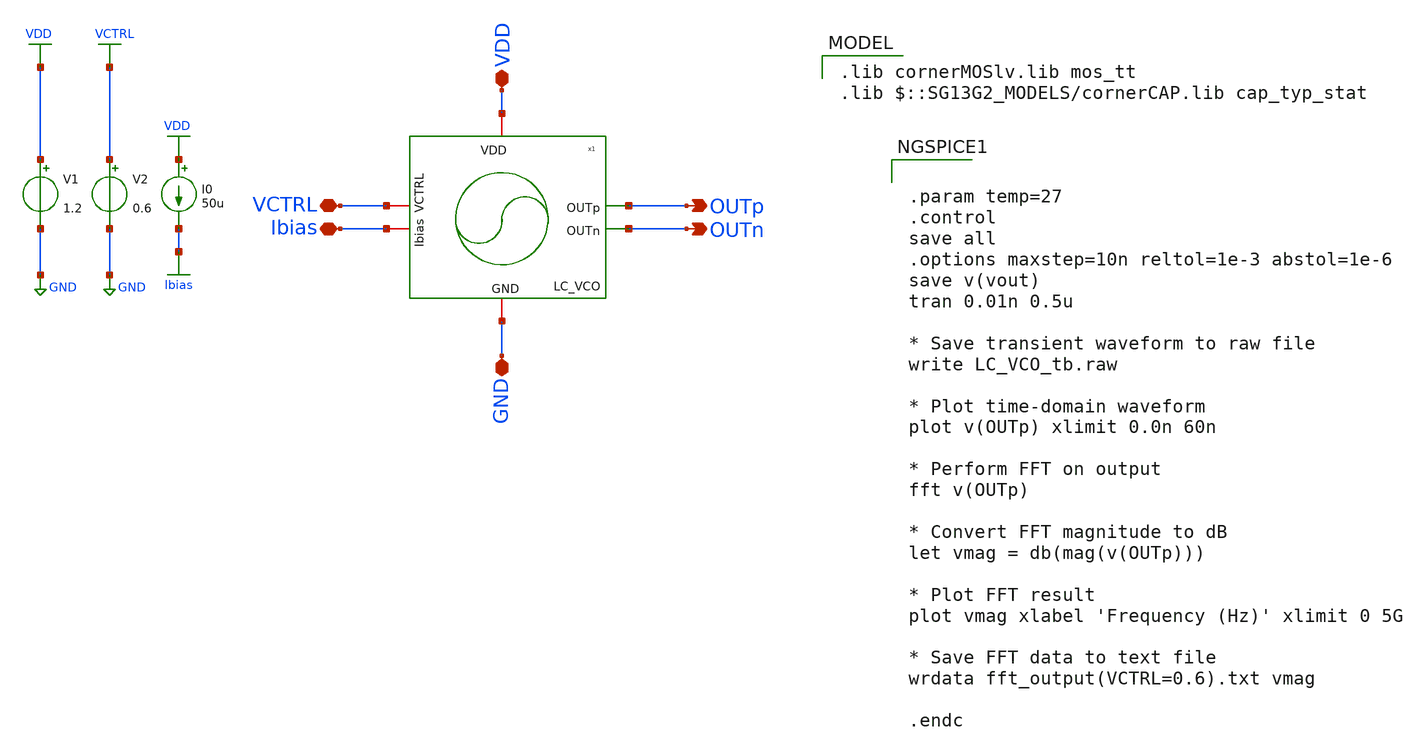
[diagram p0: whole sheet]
** sch_path: schematic/blocks/lc-vco/LC_VCO_tb.sch
**.subckt LC_VCO_tb OUTp OUTn VDD VCTRL GND Ibias
*.opin OUTp
*.opin OUTn
*.iopin VDD
*.iopin VCTRL
*.iopin GND
*.iopin Ibias
V1 VDD GND 1.2
V2 VCTRL GND 0.6
x1 VDD OUTp OUTn Ibias VCTRL GND LC_VCO
I0 VDD Ibias 50u
**** begin user architecture code
 .lib cornerMOSlv.lib mos_tt
.lib $::SG13G2_MODELS/cornerCAP.lib cap_typ_stat



.param temp=27
.control
save all
.options maxstep=10n reltol=1e-3 abstol=1e-6
save v(vout)
tran 0.01n 0.5u

* Save transient waveform to raw file
write LC_VCO_tb.raw

* Plot time-domain waveform
plot v(OUTp) xlimit 0.0n 60n

* Perform FFT on output
fft v(OUTp)

* Convert FFT magnitude to dB
let vmag = db(mag(v(OUTp)))

* Plot FFT result
plot vmag xlabel 'Frequency (Hz)' xlimit 0 5G

* Save FFT data to text file
wrdata fft_output(VCTRL=0.6).txt vmag

.endc


**** end user architecture code
**.ends

* expanding   symbol:  LC_VCO.sym # of pins=6
** sym_path: LC_VCO.sym
** sch_path: LC_VCO.sch
.subckt LC_VCO VDD OUTp OUTn Ibias VCTRL GND
*.iopin VDD
*.opin OUTp
*.opin OUTn
*.iopin GND
*.iopin VCTRL
*.iopin Ibias
L2 net2 OUTn 4n m=1
XM6 net1 Ibias GND GND sg13_lv_nmos w=1u l=0.15u ng=1 m=60 mm_ok=1
XM5 Ibias Ibias GND GND sg13_lv_nmos w=1u l=0.15u ng=1 m=1 mm_ok=1
XM4 OUTp OUTn VDD VDD sg13_lv_pmos w=8.5u l=0.5u ng=1 m=13 mm_ok=1
X5M3 OUTn OUTp VDD VDD sg13_lv_pmos w=8.5u l=0.5u ng=1 m=13 mm_ok=1
XM7 OUTp OUTn net1 GND sg13_lv_nmos w=2u l=0.5u ng=1 m=12 mm_ok=1
XM8 OUTn OUTp net1 GND sg13_lv_nmos w=2u l=0.5u ng=1 m=12 mm_ok=1
R6 OUTp OUTn 1.25k m=1
R1 OUTp net2 4 m=1
XC3 OUTp OUTn cap_cmim w=4.0e-6 l=4.0e-6 m=14.8 mm_ok=1
XMv4 OUTp VCTRL OUTp VDD sg13_lv_pmos w=4u l=4u ng=1 m=20 mm_ok=1
XMv1 OUTn VCTRL OUTn VDD sg13_lv_pmos w=4u l=4u ng=1 m=20 mm_ok=1
.ends

.GLOBAL GND
.GLOBAL VDD
.GLOBAL VCTRL
.GLOBAL Ibias
.end
